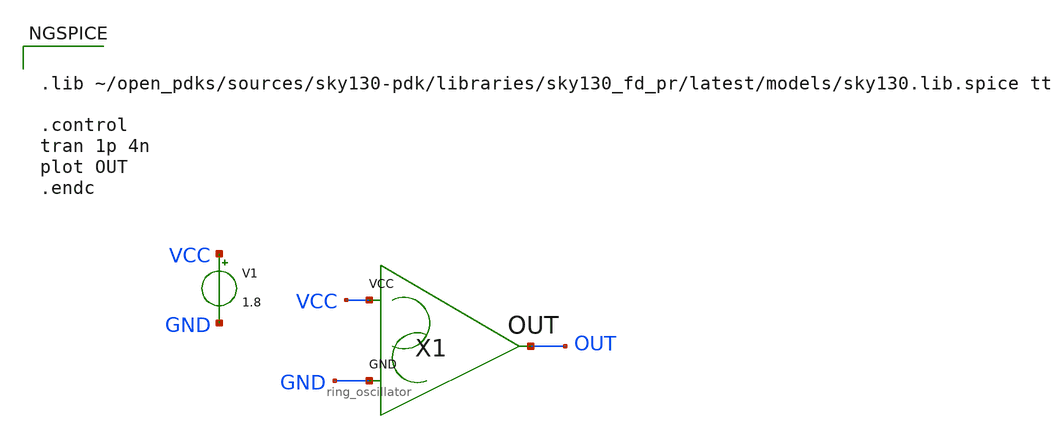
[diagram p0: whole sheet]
** sch_path: Week 4/xschem_comparator/ring_tb.sch
**.subckt ring_tb
V1 VCC GND 1.8
X1 GND VCC OUT ring_oscillator
**** begin user architecture code


.lib ~/open_pdks/sources/sky130-pdk/libraries/sky130_fd_pr/latest/models/sky130.lib.spice tt

.control
tran 1p 4n
plot OUT
.endc


**** end user architecture code
**.ends

* expanding   symbol:  ring_oscillator.sym # of pins=3
** sym_path: Week 4/xschem_comparator/ring_oscillator.sym
** sch_path: Week 4/xschem_comparator/ring_oscillator.sch
.subckt ring_oscillator GND VCC OUT
*.opin OUT
*.iopin VCC
*.iopin GND
XM1 net1 OUT VCC VCC sky130_fd_pr__pfet_01v8 L=0.15 W=1.68 nf=1 ad='int((nf+1)/2) * W/nf * 0.29' as='int((nf+2)/2) * W/nf * 0.29'
+ pd='2*int((nf+1)/2) * (W/nf + 0.29)' ps='2*int((nf+2)/2) * (W/nf + 0.29)' nrd='0.29 / W' nrs='0.29 / W'
+ sa=0 sb=0 sd=0 mult=1 m=1
XM2 net2 net1 VCC VCC sky130_fd_pr__pfet_01v8 L=0.15 W=1.68 nf=1 ad='int((nf+1)/2) * W/nf * 0.29' as='int((nf+2)/2) * W/nf * 0.29'
+ pd='2*int((nf+1)/2) * (W/nf + 0.29)' ps='2*int((nf+2)/2) * (W/nf + 0.29)' nrd='0.29 / W' nrs='0.29 / W'
+ sa=0 sb=0 sd=0 mult=1 m=1
XM3 OUT net2 VCC VCC sky130_fd_pr__pfet_01v8 L=0.15 W=1.68 nf=1 ad='int((nf+1)/2) * W/nf * 0.29' as='int((nf+2)/2) * W/nf * 0.29'
+ pd='2*int((nf+1)/2) * (W/nf + 0.29)' ps='2*int((nf+2)/2) * (W/nf + 0.29)' nrd='0.29 / W' nrs='0.29 / W'
+ sa=0 sb=0 sd=0 mult=1 m=1
XM4 net1 OUT GND GND sky130_fd_pr__nfet_01v8 L=0.15 W=1.68 nf=1 ad='int((nf+1)/2) * W/nf * 0.29' as='int((nf+2)/2) * W/nf * 0.29'
+ pd='2*int((nf+1)/2) * (W/nf + 0.29)' ps='2*int((nf+2)/2) * (W/nf + 0.29)' nrd='0.29 / W' nrs='0.29 / W'
+ sa=0 sb=0 sd=0 mult=1 m=1
XM5 net2 net1 GND GND sky130_fd_pr__nfet_01v8 L=0.15 W=1.68 nf=1 ad='int((nf+1)/2) * W/nf * 0.29' as='int((nf+2)/2) * W/nf * 0.29'
+ pd='2*int((nf+1)/2) * (W/nf + 0.29)' ps='2*int((nf+2)/2) * (W/nf + 0.29)' nrd='0.29 / W' nrs='0.29 / W'
+ sa=0 sb=0 sd=0 mult=1 m=1
XM6 OUT net2 GND GND sky130_fd_pr__nfet_01v8 L=0.15 W=1.68 nf=1 ad='int((nf+1)/2) * W/nf * 0.29' as='int((nf+2)/2) * W/nf * 0.29'
+ pd='2*int((nf+1)/2) * (W/nf + 0.29)' ps='2*int((nf+2)/2) * (W/nf + 0.29)' nrd='0.29 / W' nrs='0.29 / W'
+ sa=0 sb=0 sd=0 mult=1 m=1
.ends

.end
